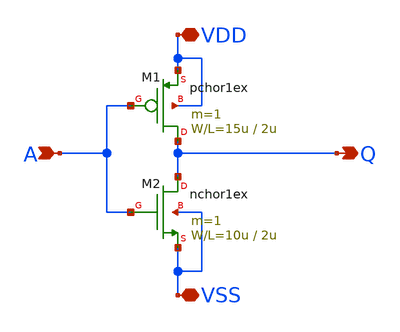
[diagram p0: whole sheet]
** sch_path: member_project/matsumoto325/myinverter1st.sch
**.subckt myinverter1st A Q VDD VSS
*.ipin A
*.opin Q
*.iopin VDD
*.iopin VSS
M1 Q A VDD VDD pchor1ex L=2u W=15u m=1
M2 Q A VSS VSS nchor1ex L=2u W=10u m=1
**.ends
.end
